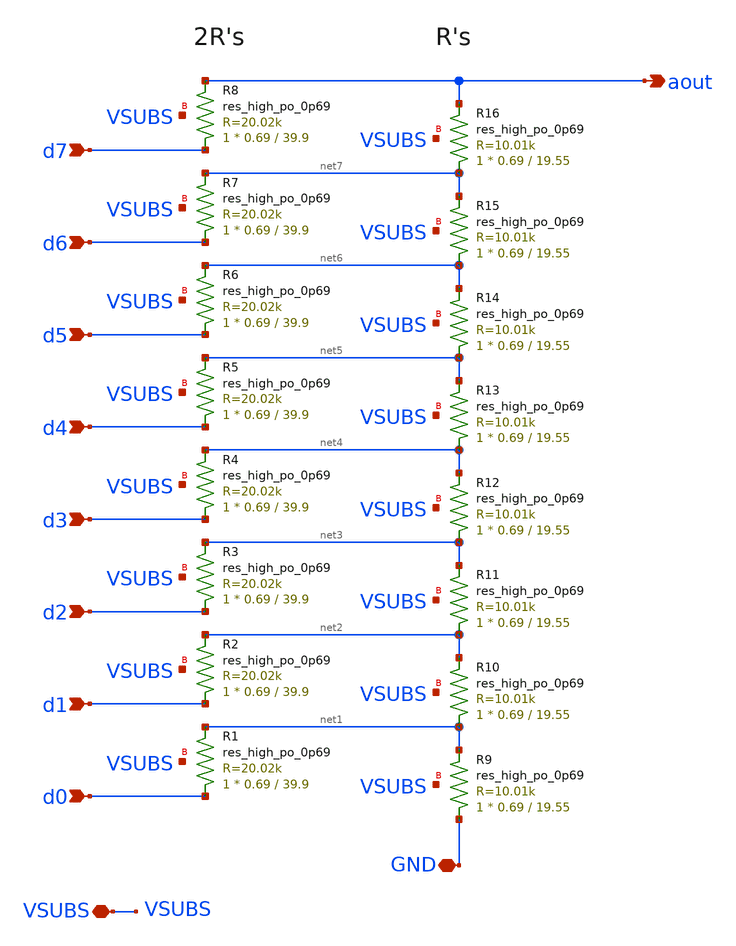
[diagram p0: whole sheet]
** sch_path: xschem/r2r.sch
**.subckt r2r d0 d1 d2 d3 d4 d5 d6 d7 GND VSUBS aout
*.ipin d0
*.ipin d1
*.ipin d2
*.ipin d3
*.ipin d4
*.ipin d5
*.ipin d6
*.ipin d7
*.iopin GND
*.iopin VSUBS
*.opin aout
XR1 d0 net1 VSUBS sky130_fd_pr__res_high_po_0p69 L=39.9 mult=1 m=1
XR2 d1 net2 VSUBS sky130_fd_pr__res_high_po_0p69 L=39.9 mult=1 m=1
XR3 d2 net3 VSUBS sky130_fd_pr__res_high_po_0p69 L=39.9 mult=1 m=1
XR4 d3 net4 VSUBS sky130_fd_pr__res_high_po_0p69 L=39.9 mult=1 m=1
XR5 d4 net5 VSUBS sky130_fd_pr__res_high_po_0p69 L=39.9 mult=1 m=1
XR6 d5 net6 VSUBS sky130_fd_pr__res_high_po_0p69 L=39.9 mult=1 m=1
XR7 d6 net7 VSUBS sky130_fd_pr__res_high_po_0p69 L=39.9 mult=1 m=1
XR8 d7 aout VSUBS sky130_fd_pr__res_high_po_0p69 L=39.9 mult=1 m=1
XR9 GND net1 VSUBS sky130_fd_pr__res_high_po_0p69 L=19.55 mult=1 m=1
XR10 net1 net2 VSUBS sky130_fd_pr__res_high_po_0p69 L=19.55 mult=1 m=1
XR11 net2 net3 VSUBS sky130_fd_pr__res_high_po_0p69 L=19.55 mult=1 m=1
XR12 net3 net4 VSUBS sky130_fd_pr__res_high_po_0p69 L=19.55 mult=1 m=1
XR13 net4 net5 VSUBS sky130_fd_pr__res_high_po_0p69 L=19.55 mult=1 m=1
XR14 net5 net6 VSUBS sky130_fd_pr__res_high_po_0p69 L=19.55 mult=1 m=1
XR15 net6 net7 VSUBS sky130_fd_pr__res_high_po_0p69 L=19.55 mult=1 m=1
XR16 net7 aout VSUBS sky130_fd_pr__res_high_po_0p69 L=19.55 mult=1 m=1
**.ends
.end
